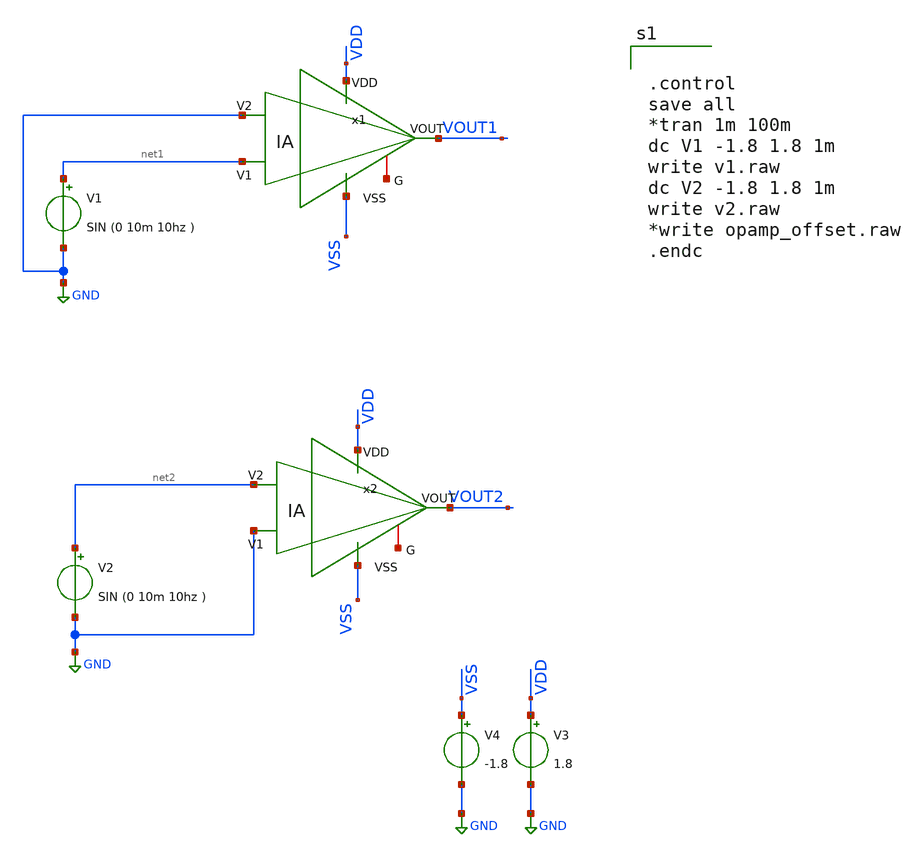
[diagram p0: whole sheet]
** sch_path: instramp_offset.sch
**.subckt instramp_offset
V1 net1 GND SIN (0 10m 10hz )
V2 net2 GND SIN (0 10m 10hz )
V4 VSS GND -1.8
V3 VDD GND 1.8
x1 VDD VSS VOUT1 net1 GND net3 IA
x2 VDD VSS VOUT2 GND net2 net4 IA
**** begin user architecture code

** opencircuitdesign pdks install
.lib $::SKYWATER_MODELS/sky130.lib.spice tt




.control
save all
*tran 1m 100m
dc V1 -1.8 1.8 1m
write v1.raw
dc V2 -1.8 1.8 1m
write v2.raw
*write opamp_offset.raw
.endc


**** end user architecture code
**.ends

* expanding   symbol:  /foss/designs/chipalooza2024/sky130_hcmus_ip__instramp/xschem/IA.sym # of
*+ pins=6
** sym_path: IA.sym
** sch_path: IA.sch
.subckt IA VDD VSS VOUT V1 V2 G
*.opin VOUT
*.iopin G
*.ipin VDD
*.ipin VSS
*.ipin V1
*.ipin V2
XR3 net1 net2 VSS sky130_fd_pr__res_high_po W=1 L=62 mult=1 m=1
XR1 net2 VOUT VSS sky130_fd_pr__res_high_po W=1 L=62 mult=1 m=1
XR2 net7 net6 VSS sky130_fd_pr__res_high_po W=1 L=62 mult=1 m=1
XR4 net6 net1 VSS sky130_fd_pr__res_high_po W=1 L=62 mult=1 m=1
XR5 net3 net4 VSS sky130_fd_pr__res_high_po W=1 L=62 mult=1 m=1
XR6 net4 G VSS sky130_fd_pr__res_high_po W=1 L=62 mult=1 m=1
XR7 net8 net5 VSS sky130_fd_pr__res_high_po W=1 L=62 mult=1 m=1
XR8 net5 net3 VSS sky130_fd_pr__res_high_po W=1 L=62 mult=1 m=1
XR9 net7 net9 VSS sky130_fd_pr__res_high_po W=1 L=62 mult=1 m=1
XR10 net9 net10 VSS sky130_fd_pr__res_high_po W=1 L=62 mult=1 m=1
XR11 net11 net12 VSS sky130_fd_pr__res_high_po W=1 L=62 mult=1 m=1
XR12 net12 net8 VSS sky130_fd_pr__res_high_po W=1 L=62 mult=1 m=1
XR13 net10 net11 VSS sky130_fd_pr__res_high_po W=1 L=62 mult=1 m=1
x1 VDD VSS V2 net10 net7 opamp
x2 VDD VSS V1 net11 net8 opamp
x3 VDD VSS net3 net1 VOUT opamp
.ends


* expanding   symbol:  ../xschem/opamp.sym # of pins=5
** sym_path: ../xschem/opamp.sym
** sch_path: ../xschem/opamp.sch
.subckt opamp VDD VSS V1 V2 VOUT
*.ipin VSS
*.ipin VDD
*.ipin V2
*.ipin V1
*.opin VOUT
XM2 net2 V2 net1 VSS sky130_fd_pr__nfet_g5v0d10v5 L=1 W=17.45 nf=1 ad='int((nf+1)/2) * W/nf * 0.29' as='int((nf+2)/2) * W/nf * 0.29'
+ pd='2*int((nf+1)/2) * (W/nf + 0.29)' ps='2*int((nf+2)/2) * (W/nf + 0.29)' nrd='0.29 / W' nrs='0.29 / W'
+ sa=0 sb=0 sd=0 mult=1 m=1
XM1 net3 net2 VDD VDD sky130_fd_pr__pfet_g5v0d10v5 L=1 W=30 nf=1 ad='int((nf+1)/2) * W/nf * 0.29' as='int((nf+2)/2) * W/nf * 0.29'
+ pd='2*int((nf+1)/2) * (W/nf + 0.29)' ps='2*int((nf+2)/2) * (W/nf + 0.29)' nrd='0.29 / W' nrs='0.29 / W'
+ sa=0 sb=0 sd=0 mult=1 m=1
XM4 net3 V1 net1 VSS sky130_fd_pr__nfet_g5v0d10v5 L=1 W=17.45 nf=1 ad='int((nf+1)/2) * W/nf * 0.29' as='int((nf+2)/2) * W/nf * 0.29'
+ pd='2*int((nf+1)/2) * (W/nf + 0.29)' ps='2*int((nf+2)/2) * (W/nf + 0.29)' nrd='0.29 / W' nrs='0.29 / W'
+ sa=0 sb=0 sd=0 mult=1 m=1
XM5 net6 net4 VSS VSS sky130_fd_pr__nfet_g5v0d10v5 L=1 W=15.17 nf=1 ad='int((nf+1)/2) * W/nf * 0.29'
+ as='int((nf+2)/2) * W/nf * 0.29' pd='2*int((nf+1)/2) * (W/nf + 0.29)' ps='2*int((nf+2)/2) * (W/nf + 0.29)'
+ nrd='0.29 / W' nrs='0.29 / W' sa=0 sb=0 sd=0 mult=1 m=1
XM6 net8 net4 VSS VSS sky130_fd_pr__nfet_g5v0d10v5 L=1 W=19 nf=1 ad='int((nf+1)/2) * W/nf * 0.29' as='int((nf+2)/2) * W/nf * 0.29'
+ pd='2*int((nf+1)/2) * (W/nf + 0.29)' ps='2*int((nf+2)/2) * (W/nf + 0.29)' nrd='0.29 / W' nrs='0.29 / W'
+ sa=0 sb=0 sd=0 mult=1 m=1
XM7 net4 net4 VSS VSS sky130_fd_pr__nfet_g5v0d10v5 L=1 W=15.17 nf=1 ad='int((nf+1)/2) * W/nf * 0.29'
+ as='int((nf+2)/2) * W/nf * 0.29' pd='2*int((nf+1)/2) * (W/nf + 0.29)' ps='2*int((nf+2)/2) * (W/nf + 0.29)'
+ nrd='0.29 / W' nrs='0.29 / W' sa=0 sb=0 sd=0 mult=1 m=1
XM3 net2 net2 VDD VDD sky130_fd_pr__pfet_g5v0d10v5 L=1 W=30 nf=1 ad='int((nf+1)/2) * W/nf * 0.29' as='int((nf+2)/2) * W/nf * 0.29'
+ pd='2*int((nf+1)/2) * (W/nf + 0.29)' ps='2*int((nf+2)/2) * (W/nf + 0.29)' nrd='0.29 / W' nrs='0.29 / W'
+ sa=0 sb=0 sd=0 mult=1 m=1
XM8 VOUT net3 VDD VDD sky130_fd_pr__pfet_g5v0d10v5 L=1 W=38 nf=1 ad='int((nf+1)/2) * W/nf * 0.29' as='int((nf+2)/2) * W/nf * 0.29'
+ pd='2*int((nf+1)/2) * (W/nf + 0.29)' ps='2*int((nf+2)/2) * (W/nf + 0.29)' nrd='0.29 / W' nrs='0.29 / W'
+ sa=0 sb=0 sd=0 mult=2 m=2
XC1 net5 net3 sky130_fd_pr__cap_mim_m3_1 W=9 L=9 MF=2 m=2
V_ibias net7 net4 0
.save i(v_ibias)
XR3 net5 VOUT VSS sky130_fd_pr__res_high_po_0p69 L=3.2 mult=1 m=1
V_ibias1 net1 net6 0
.save i(v_ibias1)
I1 net9 net10 63.26u
V_iout VOUT net8 0
.save i(v_iout)
XM9 VDD VDD net7 VSS sky130_fd_pr__nfet_g5v0d10v5 L=1 W=0.69 nf=1 ad='int((nf+1)/2) * W/nf * 0.29' as='int((nf+2)/2) * W/nf * 0.29'
+ pd='2*int((nf+1)/2) * (W/nf + 0.29)' ps='2*int((nf+2)/2) * (W/nf + 0.29)' nrd='0.29 / W' nrs='0.29 / W'
+ sa=0 sb=0 sd=0 mult=1 m=1
.ends

.GLOBAL GND
.end
